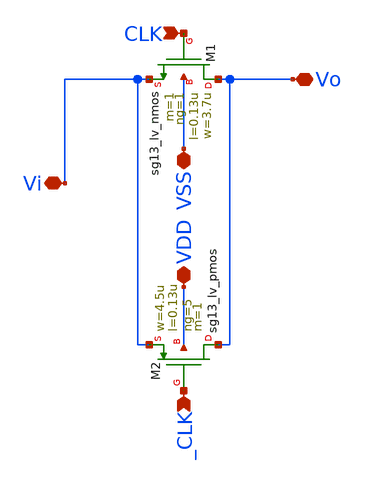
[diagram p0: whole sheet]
** sch_path: sch/blocks/sw_tg_big.sch
**.subckt sw_tg_big VSS CLK Vi Vo VDD _CLK
*.iopin VSS
*.ipin CLK
*.iopin Vi
*.iopin Vo
*.iopin VDD
*.ipin _CLK
XM1 Vo CLK Vi VSS sg13_lv_nmos w=3.7u l=0.13u ng=1 m=1 mm_ok=1
XM2 Vo _CLK Vi VDD sg13_lv_pmos w=4.5u l=0.13u ng=5 m=1 mm_ok=1
**.ends
.end
